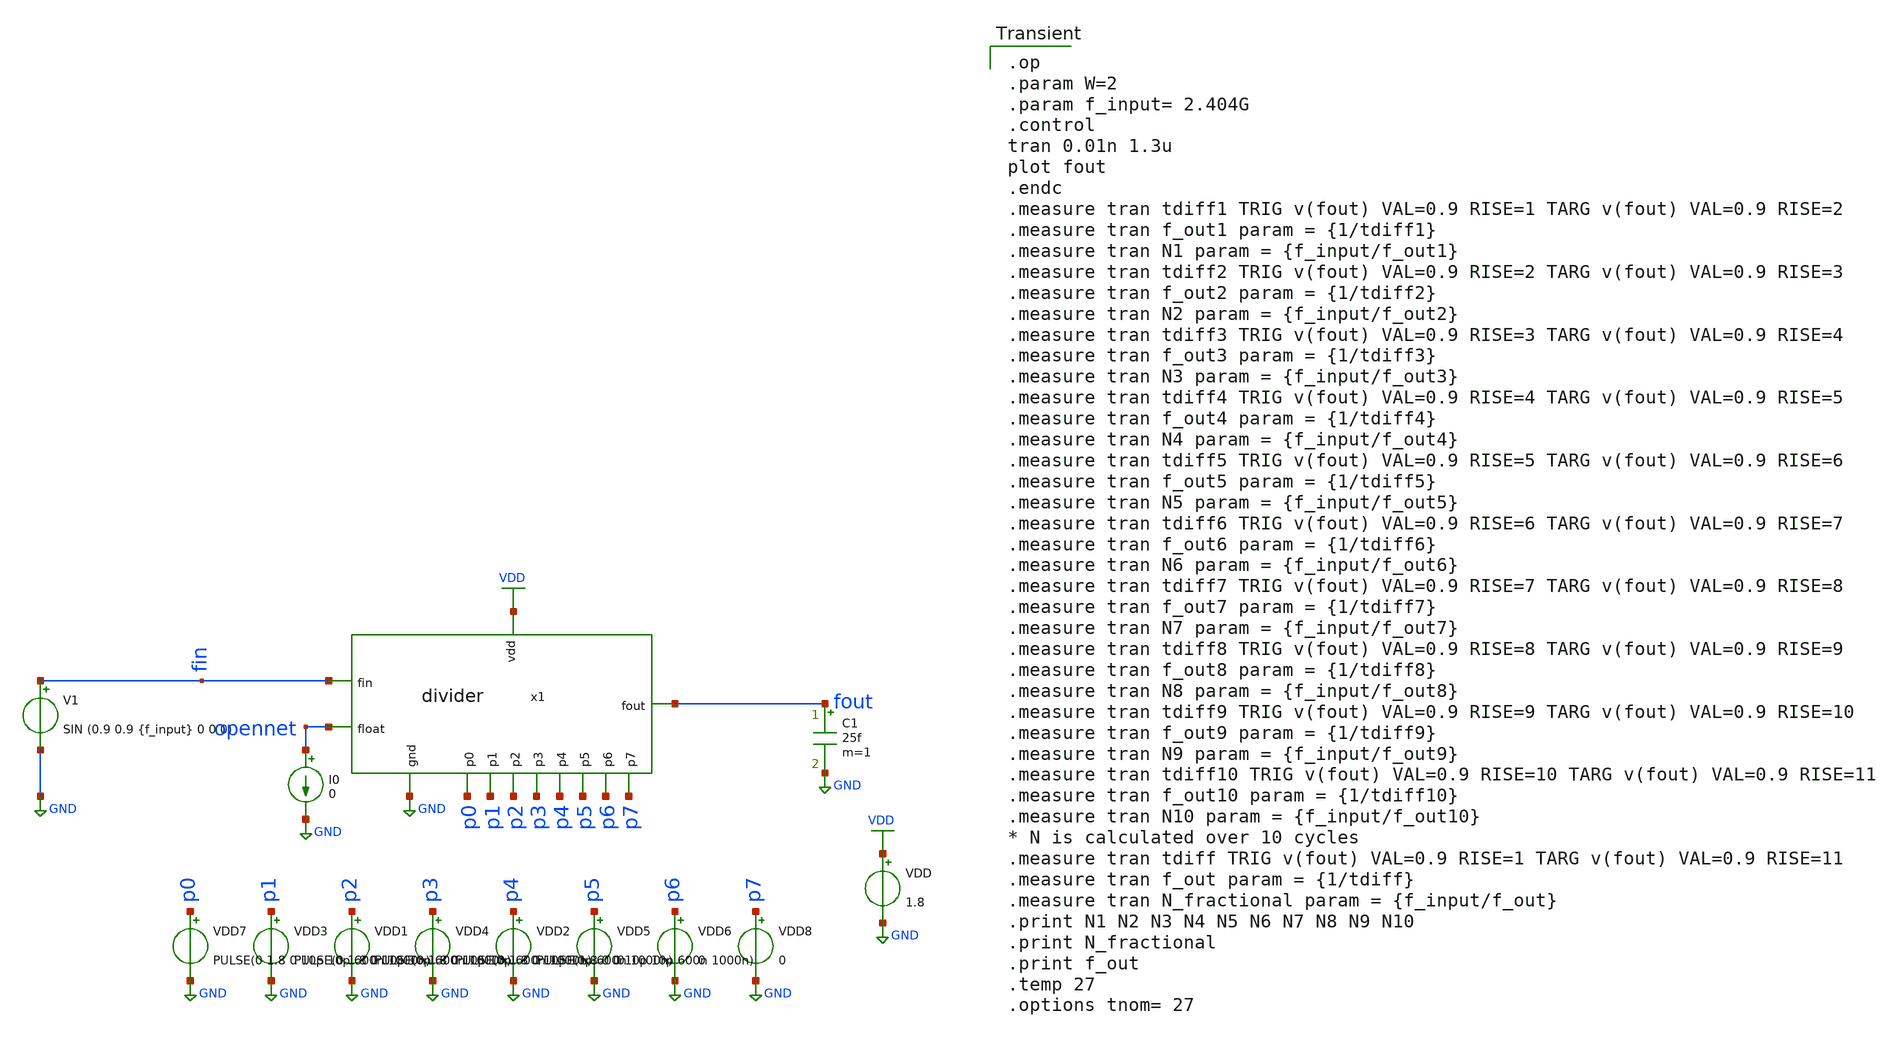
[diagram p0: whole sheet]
** sch_path: pll/dividers_lib/fractional_N_ratios/xschem/divider_tb_fractional.sch
**.subckt divider_tb_fractional
VDD VDD GND 1.8
VDD1 p2 GND PULSE(0 1.8 0 10p 10p 600n 1000n)
VDD2 p4 GND PULSE(1.8 0 0 10p 10p 600n 1000n)
VDD3 p1 GND PULSE(0 1.8 0 10p 10p 600n 1000n)
VDD4 p3 GND PULSE(0 1.8 0 10p 10p 600n 1000n)
VDD5 p5 GND 0
VDD6 p6 GND 0
VDD7 p0 GND PULSE(0 1.8 0 10p 10p 600n 1000n)
VDD8 p7 GND 0
x1 VDD fout GND p2 p7 p1 p6 p5 p4 p3 p0 fin opennet divider
V1 fin GND SIN (0.9 0.9 {f_input} 0 0 0)
C1 fout GND 25f m=1
I0 opennet GND 0
**** begin user architecture code

.op
.param W=2
.param f_input= 2.404G
.control
tran 0.01n 1.3u
plot fout
.endc
.measure tran tdiff1 TRIG v(fout) VAL=0.9 RISE=1 TARG v(fout) VAL=0.9 RISE=2
.measure tran f_out1 param = {1/tdiff1}
.measure tran N1 param = {f_input/f_out1}
.measure tran tdiff2 TRIG v(fout) VAL=0.9 RISE=2 TARG v(fout) VAL=0.9 RISE=3
.measure tran f_out2 param = {1/tdiff2}
.measure tran N2 param = {f_input/f_out2}
.measure tran tdiff3 TRIG v(fout) VAL=0.9 RISE=3 TARG v(fout) VAL=0.9 RISE=4
.measure tran f_out3 param = {1/tdiff3}
.measure tran N3 param = {f_input/f_out3}
.measure tran tdiff4 TRIG v(fout) VAL=0.9 RISE=4 TARG v(fout) VAL=0.9 RISE=5
.measure tran f_out4 param = {1/tdiff4}
.measure tran N4 param = {f_input/f_out4}
.measure tran tdiff5 TRIG v(fout) VAL=0.9 RISE=5 TARG v(fout) VAL=0.9 RISE=6
.measure tran f_out5 param = {1/tdiff5}
.measure tran N5 param = {f_input/f_out5}
.measure tran tdiff6 TRIG v(fout) VAL=0.9 RISE=6 TARG v(fout) VAL=0.9 RISE=7
.measure tran f_out6 param = {1/tdiff6}
.measure tran N6 param = {f_input/f_out6}
.measure tran tdiff7 TRIG v(fout) VAL=0.9 RISE=7 TARG v(fout) VAL=0.9 RISE=8
.measure tran f_out7 param = {1/tdiff7}
.measure tran N7 param = {f_input/f_out7}
.measure tran tdiff8 TRIG v(fout) VAL=0.9 RISE=8 TARG v(fout) VAL=0.9 RISE=9
.measure tran f_out8 param = {1/tdiff8}
.measure tran N8 param = {f_input/f_out8}
.measure tran tdiff9 TRIG v(fout) VAL=0.9 RISE=9 TARG v(fout) VAL=0.9 RISE=10
.measure tran f_out9 param = {1/tdiff9}
.measure tran N9 param = {f_input/f_out9}
.measure tran tdiff10 TRIG v(fout) VAL=0.9 RISE=10 TARG v(fout) VAL=0.9 RISE=11
.measure tran f_out10 param = {1/tdiff10}
.measure tran N10 param = {f_input/f_out10}
* N is calculated over 10 cycles
.measure tran tdiff TRIG v(fout) VAL=0.9 RISE=1 TARG v(fout) VAL=0.9 RISE=11
.measure tran f_out param = {1/tdiff}
.measure tran N_fractional param = {f_input/f_out}
.print N1 N2 N3 N4 N5 N6 N7 N8 N9 N10
.print N_fractional
.print f_out
.temp 27
.options tnom= 27


** opencircuitdesign pdks install
.lib $::SKYWATER_MODELS/sky130.lib.spice tt


**** end user architecture code
**.ends
.GLOBAL VDD
.GLOBAL GND
.end
